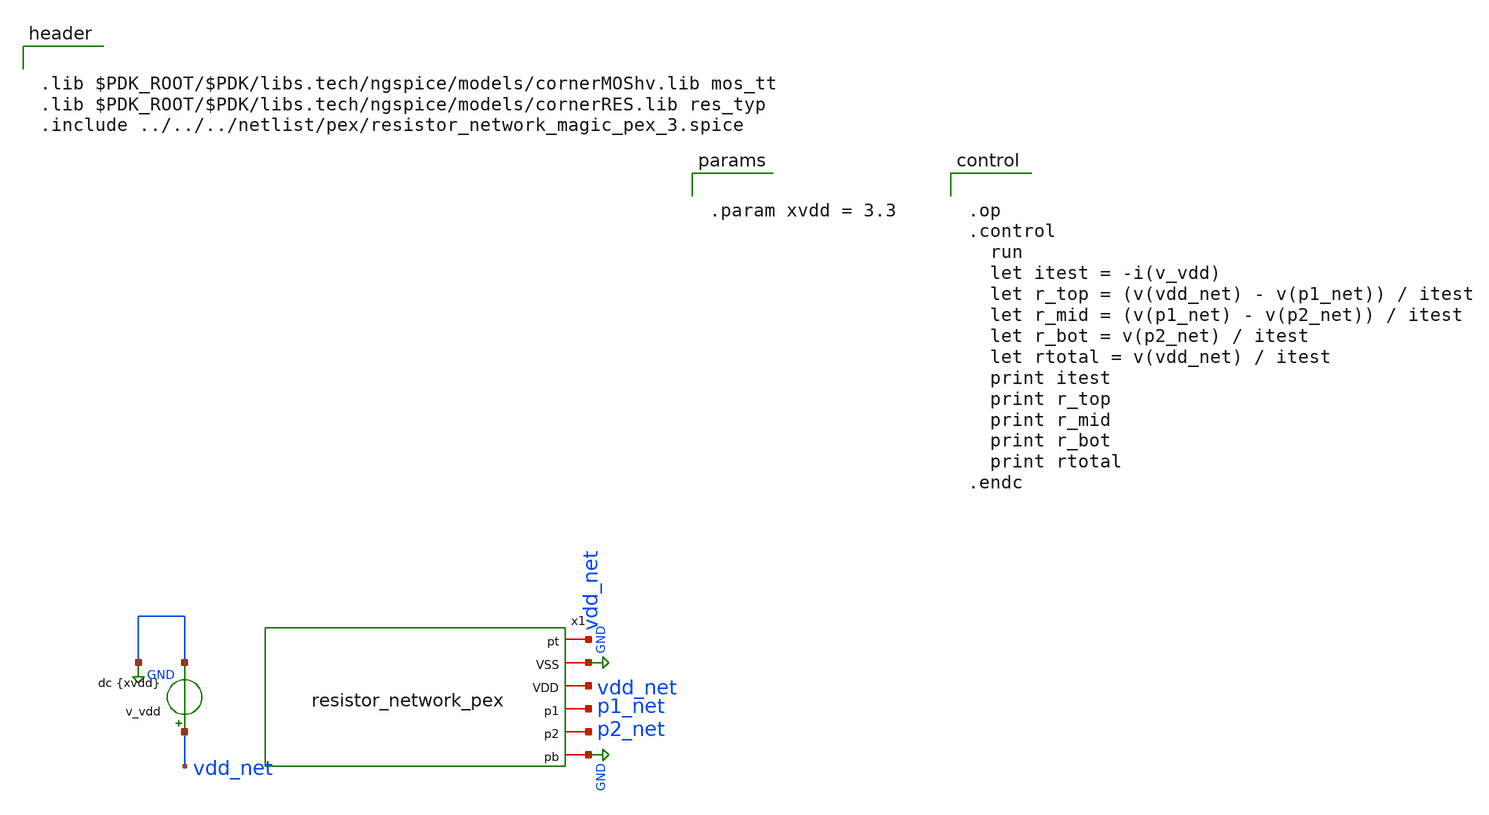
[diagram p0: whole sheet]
** sch_path: macros/resistor_network/testbenches/xschem/tb_resistor_network_pex.sch
**.subckt tb_resistor_network_pex
v_vdd vdd_net GND dc {xvdd}
x1 vdd_net GND vdd_net p1_net p2_net GND resistor_network_pex
**** begin user architecture code


.lib $PDK_ROOT/$PDK/libs.tech/ngspice/models/cornerMOShv.lib mos_tt
.lib $PDK_ROOT/$PDK/libs.tech/ngspice/models/cornerRES.lib res_typ
.include ../../../netlist/pex/resistor_network_magic_pex_3.spice




.op
.control
  run
  let itest = -i(v_vdd)
  let r_top = (v(vdd_net) - v(p1_net)) / itest
  let r_mid = (v(p1_net) - v(p2_net)) / itest
  let r_bot = v(p2_net) / itest
  let rtotal = v(vdd_net) / itest
  print itest
  print r_top
  print r_mid
  print r_bot
  print rtotal
.endc




.param xvdd = 3.3


**** end user architecture code
**.ends
.GLOBAL GND
.end
